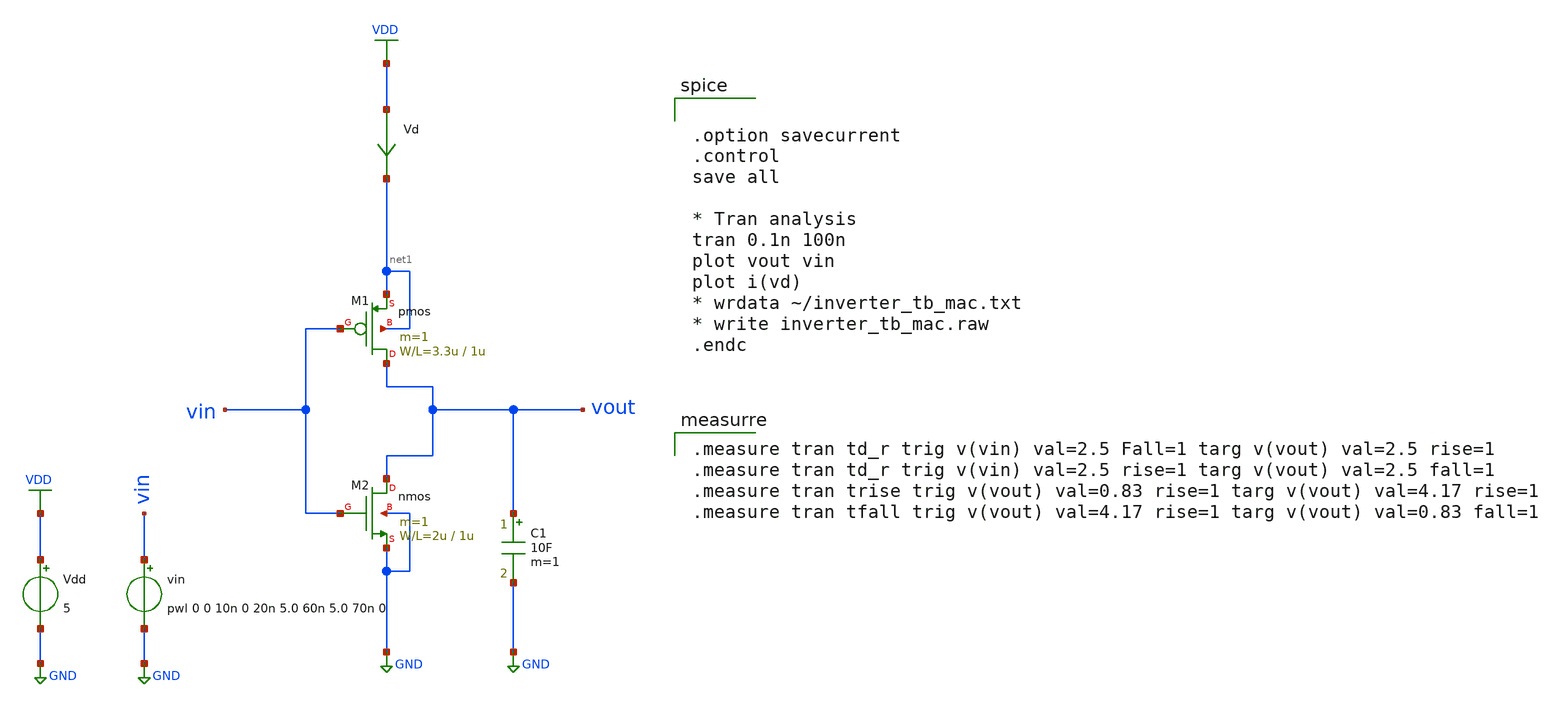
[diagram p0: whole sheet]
** sch_path: member_project/YutakaKOTANI/tb_inv_yutaka_03_trans.sch
**.subckt tb_inv_yutaka_03_trans
M1 vout vin net1 net1 pmos L=1u W=3.3u m=1
M2 vout vin GND GND nmos L=1u W=2u m=1
Vd VDD net1 0
.save i(vd)
C1 vout GND 10F m=1
Vdd VDD GND 5
vin vin GND pwl 0 0 10n 0 20n 5.0 60n 5.0 70n 0
**** begin user architecture code
 .include $::LIB/mos.lib
.include $::LIB/passive.lib
.include $::LIB/diode.lib


.option savecurrent
.control
save all

* Tran analysis
tran 0.1n 100n
plot vout vin
plot i(vd)
* wrdata ~/inverter_tb_mac.txt
* write inverter_tb_mac.raw
.endc



.measure tran td_r trig v(vin) val=2.5 Fall=1 targ v(vout) val=2.5 rise=1
.measure tran td_r trig v(vin) val=2.5 rise=1 targ v(vout) val=2.5 fall=1
.measure tran trise trig v(vout) val=0.83 rise=1 targ v(vout) val=4.17 rise=1
.measure tran tfall trig v(vout) val=4.17 rise=1 targ v(vout) val=0.83 fall=1



**** end user architecture code
**.ends
.GLOBAL VDD
.GLOBAL GND
.end
